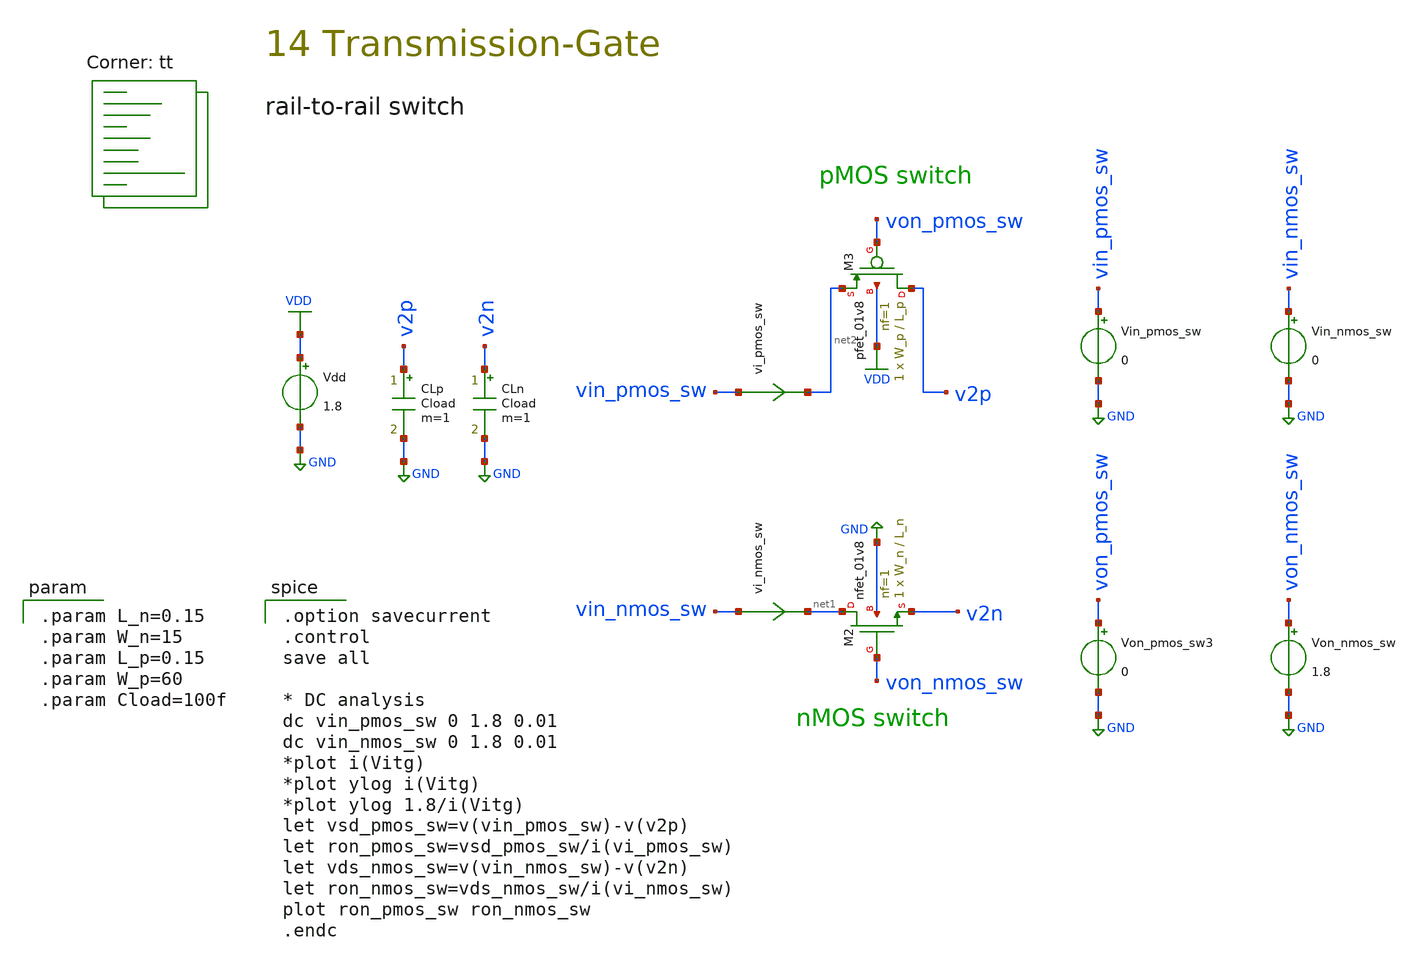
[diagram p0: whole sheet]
** sch_path: tseng_workspace/transmission_gate/schematic/spice/tg_dc_tb2.sch
**.subckt tg_dc_tb2
Vdd VDD GND 1.8
XM2 net1 von_nmos_sw v2n GND sky130_fd_pr__nfet_01v8 L=L_n W=W_n nf=1 ad='int((1 + 1)/2) * W_n / 1 * 0.29'
+ as='int((1 + 2)/2) * W_n / 1 * 0.29' pd='2*int((1 + 1)/2) * (W_n / 1 + 0.29)' ps='2*int((1 + 2)/2) * (W_n / 1 + 0.29)'
+ nrd='0.29 / W_n ' nrs='0.29 / W_n ' sa=0 sb=0 sd=0 mult=1 m=1
vi_nmos_sw vin_nmos_sw net1 0
.save i(vi_nmos_sw)
Vin_pmos_sw vin_pmos_sw GND 0
Vin_nmos_sw vin_nmos_sw GND 0
Von_pmos_sw3 von_pmos_sw GND 0
Von_nmos_sw von_nmos_sw GND 1.8
XM3 v2p von_pmos_sw net2 VDD sky130_fd_pr__pfet_01v8 L=L_p W=W_p nf=1 ad='int((nf+1)/2) * W/nf * 0.29'
+ as='int((nf+2)/2) * W/nf * 0.29' pd='2*int((nf+1)/2) * (W/nf + 0.29)' ps='2*int((nf+2)/2) * (W/nf + 0.29)'
+ nrd='0.29 / W' nrs='0.29 / W' sa=0 sb=0 sd=0 mult=1 m=1
vi_pmos_sw vin_pmos_sw net2 0
.save i(vi_pmos_sw)
CLp v2p GND Cload m=1
CLn v2n GND Cload m=1
**** begin user architecture code
.lib $::SKYWATER_MODELS/sky130.lib.spice tt

.option savecurrent
.control
save all

* DC analysis
dc vin_pmos_sw 0 1.8 0.01
dc vin_nmos_sw 0 1.8 0.01
*plot i(Vitg)
*plot ylog i(Vitg)
*plot ylog 1.8/i(Vitg)
let vsd_pmos_sw=v(vin_pmos_sw)-v(v2p)
let ron_pmos_sw=vsd_pmos_sw/i(vi_pmos_sw)
let vds_nmos_sw=v(vin_nmos_sw)-v(v2n)
let ron_nmos_sw=vds_nmos_sw/i(vi_nmos_sw)
plot ron_pmos_sw ron_nmos_sw
.endc


.param L_n=0.15
.param W_n=15
.param L_p=0.15
.param W_p=60
.param Cload=100f

**** end user architecture code
**.ends
.GLOBAL GND
.GLOBAL VDD
.end
